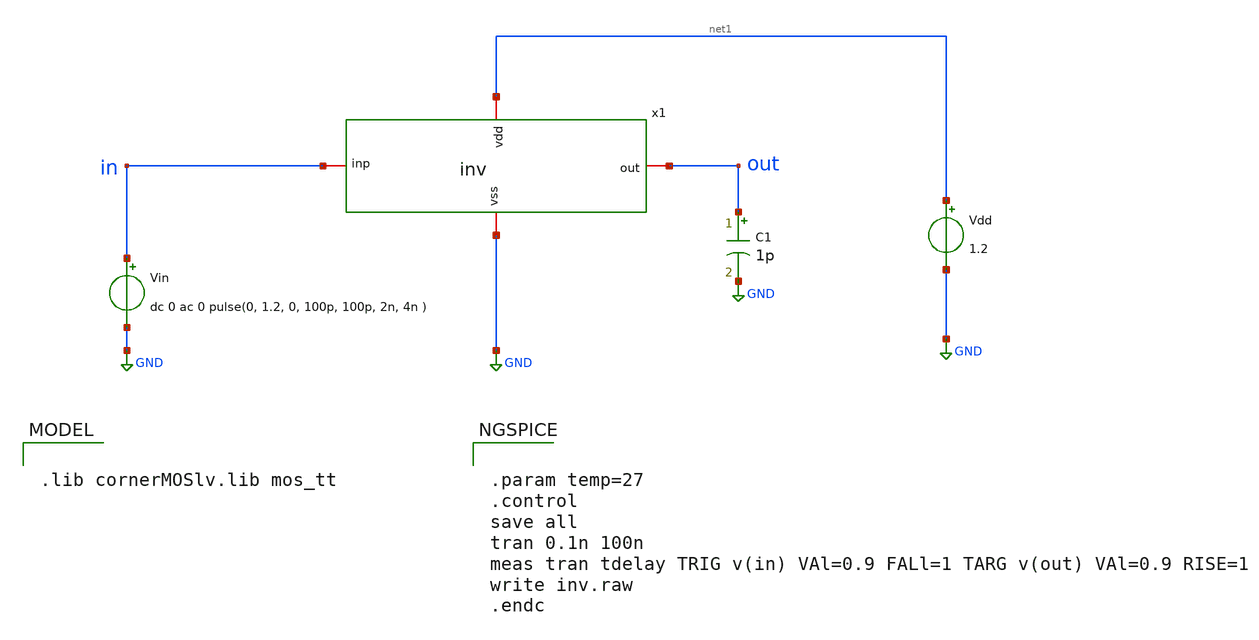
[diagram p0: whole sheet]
** sch_path: xschem/inv_tb.sch
**.subckt inv_tb
Vin in GND dc 0 ac 0 pulse(0, 1.2, 0, 100p, 100p, 2n, 4n )
Vdd net1 GND 1.2
x1 net1 in out GND inv
C1 out GND 1p m=1
**** begin user architecture code


.param temp=27
.control
save all
tran 0.1n 100n
meas tran tdelay TRIG v(in) VAl=0.9 FALl=1 TARG v(out) VAl=0.9 RISE=1
write inv.raw
.endc



.lib cornerMOSlv.lib mos_tt

**** end user architecture code
**.ends

* expanding   symbol:  inv.sym # of pins=4
** sym_path: xschem/inv.sym
** sch_path: xschem/inv.sch
.subckt inv vdd inp out vss
*.iopin vss
*.iopin out
*.iopin inp
*.iopin vdd
XM1 out inp vss vss sg13_lv_nmos w=1.0u l=0.72u ng=1 m=1 rfmode=1 mm_ok=1
XM2 out inp vdd vdd sg13_lv_pmos w=5.0u l=0.72u ng=1 m=1 rfmode=1 mm_ok=1
.ends

.GLOBAL GND
.end
